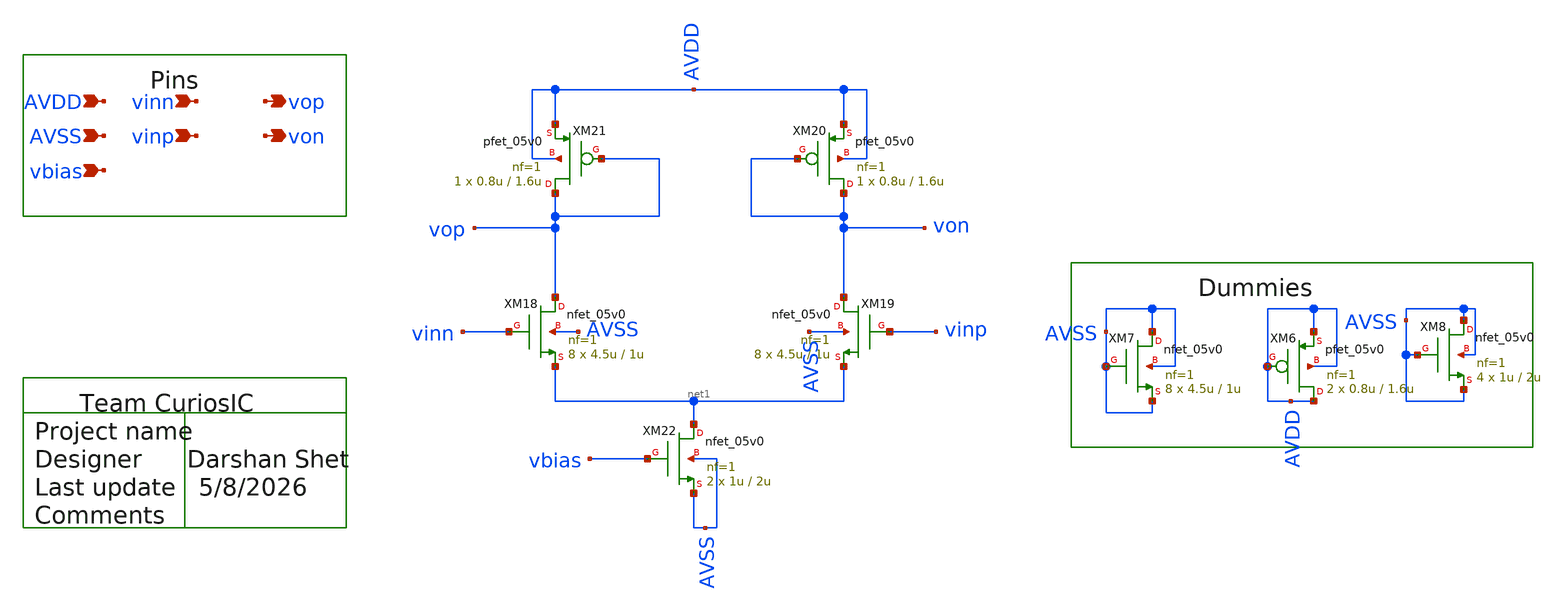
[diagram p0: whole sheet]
** sch_path: design/schematics/ADC/DSM_Loop_filter/First_int/OTA_Files/DS_cic_bms_afe_iadc_first_int_OTA_CMFB.sch
**.subckt DS_cic_bms_afe_iadc_first_int_OTA_CMFB AVDD AVSS vinn vinp vbias vop von
*.ipin AVDD
*.ipin AVSS
*.ipin vinn
*.ipin vinp
*.ipin vbias
*.opin vop
*.opin von
XM18 vop vinn net1 AVSS nfet_05v0 L=1u W=4.5u nf=1 ad='int((nf+1)/2) * W/nf * 0.18u' as='int((nf+2)/2) * W/nf * 0.18u'
+ pd='2*int((nf+1)/2) * (W/nf + 0.18u)' ps='2*int((nf+2)/2) * (W/nf + 0.18u)' nrd='0.18u / W' nrs='0.18u / W'
+ sa=0 sb=0 sd=0 m=8
XM19 von vinp net1 AVSS nfet_05v0 L=1u W=4.5u nf=1 ad='int((nf+1)/2) * W/nf * 0.18u' as='int((nf+2)/2) * W/nf * 0.18u'
+ pd='2*int((nf+1)/2) * (W/nf + 0.18u)' ps='2*int((nf+2)/2) * (W/nf + 0.18u)' nrd='0.18u / W' nrs='0.18u / W'
+ sa=0 sb=0 sd=0 m=8
XM20 von von AVDD AVDD pfet_05v0 L=1.6u W=0.8u nf=1 ad='int((nf+1)/2) * W/nf * 0.18u' as='int((nf+2)/2) * W/nf * 0.18u'
+ pd='2*int((nf+1)/2) * (W/nf + 0.18u)' ps='2*int((nf+2)/2) * (W/nf + 0.18u)' nrd='0.18u / W' nrs='0.18u / W'
+ sa=0 sb=0 sd=0 m=1
XM21 vop vop AVDD AVDD pfet_05v0 L=1.6u W=0.8u nf=1 ad='int((nf+1)/2) * W/nf * 0.18u' as='int((nf+2)/2) * W/nf * 0.18u'
+ pd='2*int((nf+1)/2) * (W/nf + 0.18u)' ps='2*int((nf+2)/2) * (W/nf + 0.18u)' nrd='0.18u / W' nrs='0.18u / W'
+ sa=0 sb=0 sd=0 m=1
XM22 net1 vbias AVSS AVSS nfet_05v0 L=2u W=1u nf=1 ad='int((nf+1)/2) * W/nf * 0.18u' as='int((nf+2)/2) * W/nf * 0.18u'
+ pd='2*int((nf+1)/2) * (W/nf + 0.18u)' ps='2*int((nf+2)/2) * (W/nf + 0.18u)' nrd='0.18u / W' nrs='0.18u / W'
+ sa=0 sb=0 sd=0 m=2
XM6 AVDD AVDD AVDD AVDD pfet_05v0 L=1.6u W=0.8u nf=1 ad='int((nf+1)/2) * W/nf * 0.18u' as='int((nf+2)/2) * W/nf * 0.18u'
+ pd='2*int((nf+1)/2) * (W/nf + 0.18u)' ps='2*int((nf+2)/2) * (W/nf + 0.18u)' nrd='0.18u / W' nrs='0.18u / W'
+ sa=0 sb=0 sd=0 m=2
XM7 AVSS AVSS AVSS AVSS nfet_05v0 L=1u W=4.5u nf=1 ad='int((nf+1)/2) * W/nf * 0.18u' as='int((nf+2)/2) * W/nf * 0.18u'
+ pd='2*int((nf+1)/2) * (W/nf + 0.18u)' ps='2*int((nf+2)/2) * (W/nf + 0.18u)' nrd='0.18u / W' nrs='0.18u / W'
+ sa=0 sb=0 sd=0 m=8
XM8 AVSS AVSS AVSS AVSS nfet_05v0 L=2u W=1u nf=1 ad='int((nf+1)/2) * W/nf * 0.18u' as='int((nf+2)/2) * W/nf * 0.18u'
+ pd='2*int((nf+1)/2) * (W/nf + 0.18u)' ps='2*int((nf+2)/2) * (W/nf + 0.18u)' nrd='0.18u / W' nrs='0.18u / W'
+ sa=0 sb=0 sd=0 m=4
**.ends
.end
